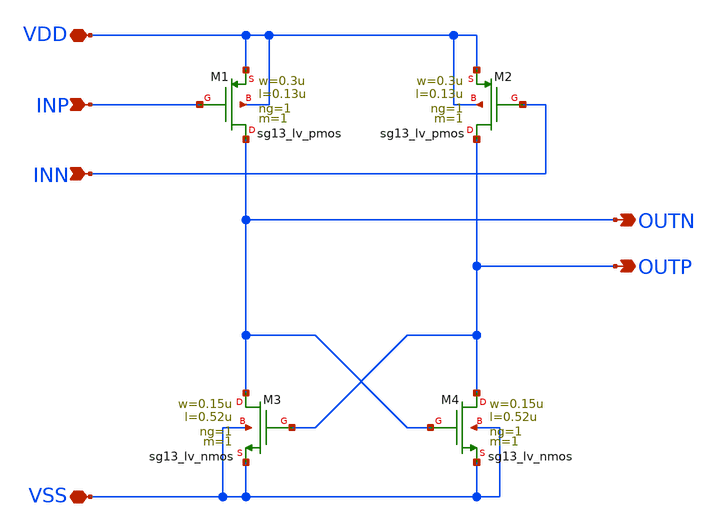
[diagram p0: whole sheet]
** sch_path: xschem/nonoverlap.sch
**.subckt nonoverlap VSS VDD INP INN OUTP OUTN
*.iopin VSS
*.iopin VDD
*.ipin INP
*.ipin INN
*.opin OUTP
*.opin OUTN
XM1 OUTN INP VDD VDD sg13_lv_pmos w=0.3u l=0.13u ng=1 m=1 mm_ok=1
XM2 OUTP INN VDD VDD sg13_lv_pmos w=0.3u l=0.13u ng=1 m=1 mm_ok=1
XM3 OUTN OUTP VSS VSS sg13_lv_nmos w=0.15u l=0.52u ng=1 m=1 mm_ok=1
XM4 OUTP OUTN VSS VSS sg13_lv_nmos w=0.15u l=0.52u ng=1 m=1 mm_ok=1
**.ends
.end
